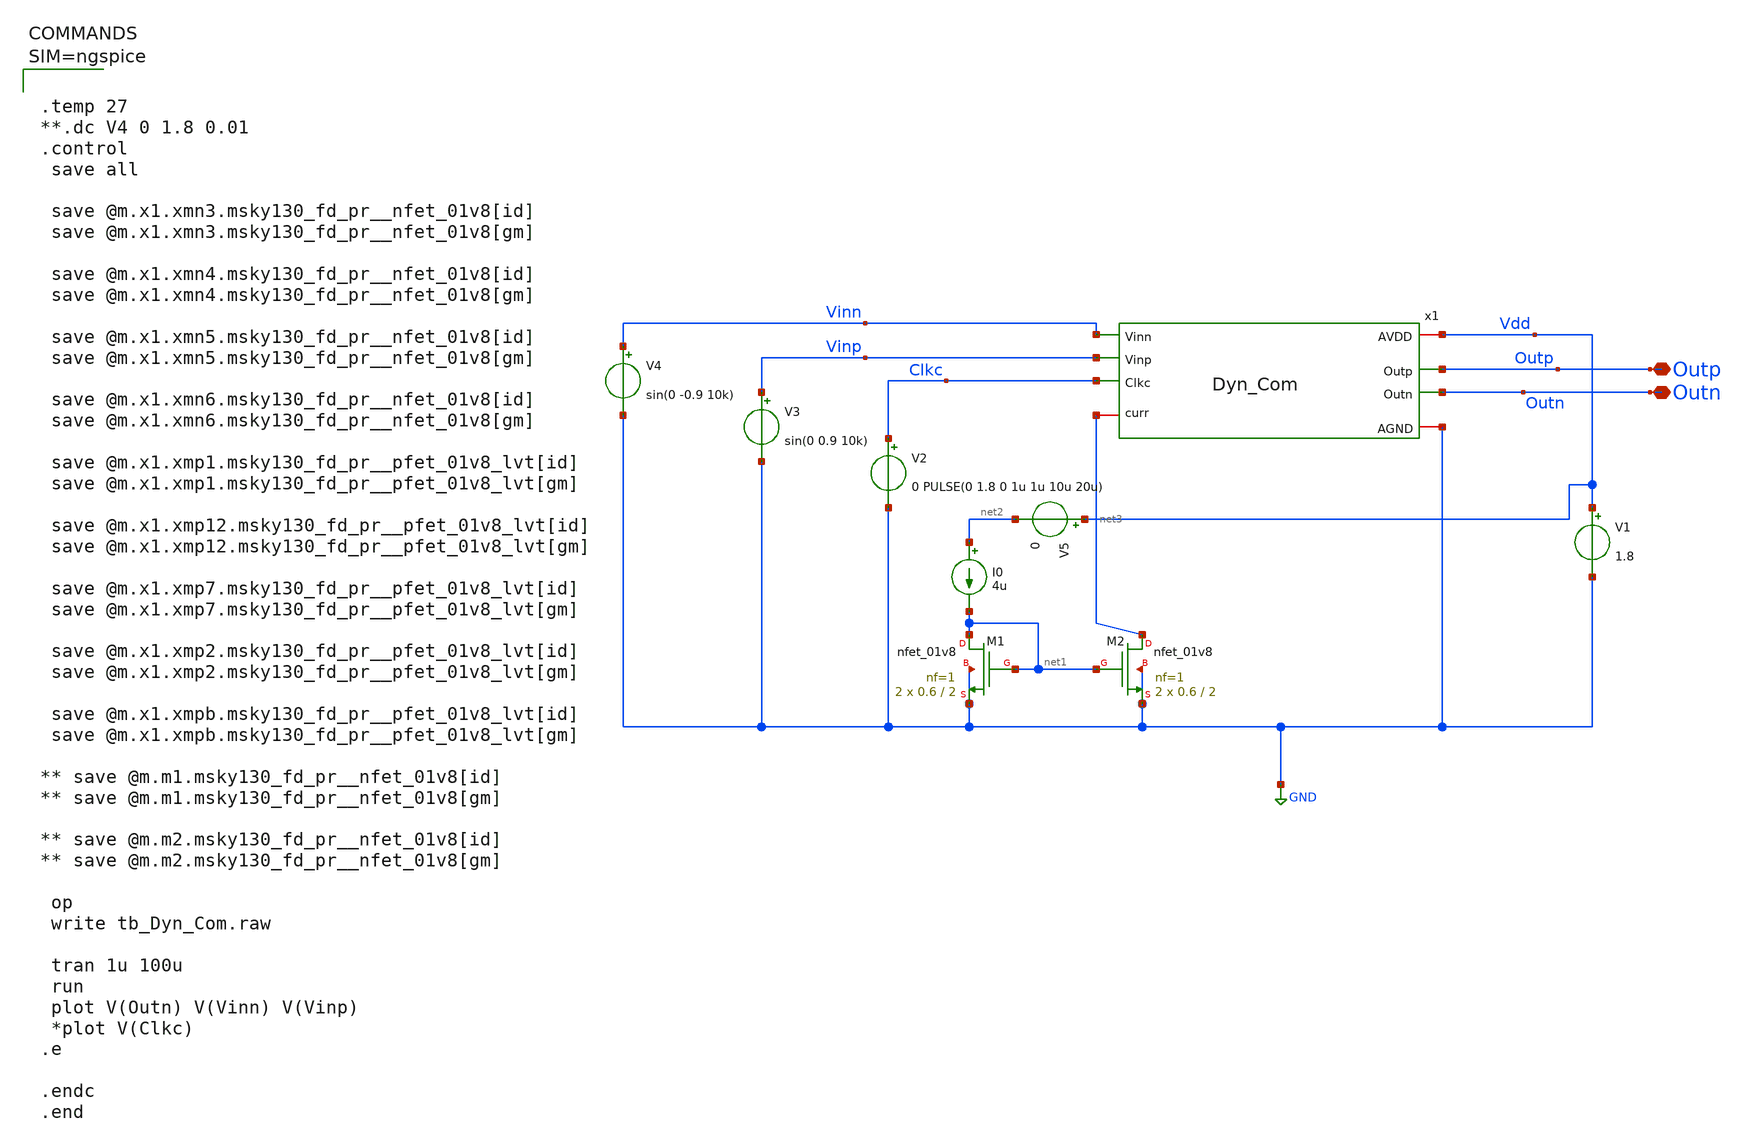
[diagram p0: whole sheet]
** sch_path: sar-adc/updated/tb_Dyn_Com.sch
**.subckt tb_Dyn_Com Outp Outn
*.iopin Outp
*.iopin Outn
x1 Vdd net3 Vinn Vinp Outp Outn Clkc GND Dyn_Com
V4 Vinn GND sin(0 -0.9 10k)
V3 Vinp GND sin(0 0.9 10k)
V2 Clkc GND 0 PULSE(0 1.8 0 1u 1u 10u 20u)
XM2 net3 net1 GND GND sky130_fd_pr__nfet_01v8 L=2 W=0.6 nf=1 ad='int((1 + 1)/2) * 0.6 / 1 * 0.29' as='int((1 + 2)/2) * 0.6 / 1 * 0.29'
+ pd='2*int((1 + 1)/2) * (0.6 / 1 + 0.29)' ps='2*int((1 + 2)/2) * (0.6 / 1 + 0.29)' nrd='0.29 / 0.6 ' nrs='0.29 / 0.6 '
+ sa=0 sb=0 sd=0 mult=2 m=2
XM1 net1 net1 GND GND sky130_fd_pr__nfet_01v8 L=2 W=0.6 nf=1 ad='int((1 + 1)/2) * 0.6 / 1 * 0.29' as='int((1 + 2)/2) * 0.6 / 1 * 0.29'
+ pd='2*int((1 + 1)/2) * (0.6 / 1 + 0.29)' ps='2*int((1 + 2)/2) * (0.6 / 1 + 0.29)' nrd='0.29 / 0.6 ' nrs='0.29 / 0.6 '
+ sa=0 sb=0 sd=0 mult=2 m=2
I0 net2 net1 4u
V5 Vdd net2 0
V1 Vdd GND 1.8
**** begin user architecture code



.temp 27
**.dc V4 0 1.8 0.01
.control
 save all

 save @m.x1.xmn3.msky130_fd_pr__nfet_01v8[id]
 save @m.x1.xmn3.msky130_fd_pr__nfet_01v8[gm]

 save @m.x1.xmn4.msky130_fd_pr__nfet_01v8[id]
 save @m.x1.xmn4.msky130_fd_pr__nfet_01v8[gm]

 save @m.x1.xmn5.msky130_fd_pr__nfet_01v8[id]
 save @m.x1.xmn5.msky130_fd_pr__nfet_01v8[gm]

 save @m.x1.xmn6.msky130_fd_pr__nfet_01v8[id]
 save @m.x1.xmn6.msky130_fd_pr__nfet_01v8[gm]

 save @m.x1.xmp1.msky130_fd_pr__pfet_01v8_lvt[id]
 save @m.x1.xmp1.msky130_fd_pr__pfet_01v8_lvt[gm]

 save @m.x1.xmp12.msky130_fd_pr__pfet_01v8_lvt[id]
 save @m.x1.xmp12.msky130_fd_pr__pfet_01v8_lvt[gm]

 save @m.x1.xmp7.msky130_fd_pr__pfet_01v8_lvt[id]
 save @m.x1.xmp7.msky130_fd_pr__pfet_01v8_lvt[gm]

 save @m.x1.xmp2.msky130_fd_pr__pfet_01v8_lvt[id]
 save @m.x1.xmp2.msky130_fd_pr__pfet_01v8_lvt[gm]

 save @m.x1.xmpb.msky130_fd_pr__pfet_01v8_lvt[id]
 save @m.x1.xmpb.msky130_fd_pr__pfet_01v8_lvt[gm]

** save @m.m1.msky130_fd_pr__nfet_01v8[id]
** save @m.m1.msky130_fd_pr__nfet_01v8[gm]

** save @m.m2.msky130_fd_pr__nfet_01v8[id]
** save @m.m2.msky130_fd_pr__nfet_01v8[gm]

 op
 write tb_Dyn_Com.raw

 tran 1u 100u
 run
 plot V(Outn) V(Vinn) V(Vinp)
 *plot V(Clkc)
.e

.endc
.end




** opencircuitdesign pdks install
.lib $::SKYWATER_MODELS/sky130.lib.spice tt

**** end user architecture code
**.ends

* expanding   symbol:  Dyn_Com.sym # of pins=8
** sym_path: sar-adc/updated/Dyn_Com.sym
** sch_path: sar-adc/updated/Dyn_Com.sch
.subckt Dyn_Com AVDD curr Vinn Vinp Outp Outn Clkc AGND
*.ipin Vinp
*.ipin Vinn
*.opin Outn
*.opin Outp
*.ipin Clkc
*.iopin AVDD
*.iopin AGND
*.iopin curr
XMPB net1 curr AVDD AVDD sky130_fd_pr__pfet_01v8_lvt L=2 W=1.12 nf=1 ad='int((1 + 1)/2) * 1.12 / 1 * 0.29'
+ as='int((1 + 2)/2) * 1.12 / 1 * 0.29' pd='2*int((1 + 1)/2) * (1.12 / 1 + 0.29)' ps='2*int((1 + 2)/2) * (1.12 / 1 + 0.29)'
+ nrd='0.29 / 1.12 ' nrs='0.29 / 1.12 ' sa=0 sb=0 sd=0 mult=4 m=4
XMP7 net2 Clkc net1 AVDD sky130_fd_pr__pfet_01v8_lvt L=2 W=1.12 nf=1 ad='int((1 + 1)/2) * 1.12 / 1 * 0.29'
+ as='int((1 + 2)/2) * 1.12 / 1 * 0.29' pd='2*int((1 + 1)/2) * (1.12 / 1 + 0.29)' ps='2*int((1 + 2)/2) * (1.12 / 1 + 0.29)'
+ nrd='0.29 / 1.12 ' nrs='0.29 / 1.12 ' sa=0 sb=0 sd=0 mult=4 m=4
XMP12 curr curr AVDD AVDD sky130_fd_pr__pfet_01v8_lvt L=2 W=1.12 nf=1 ad='int((1 + 1)/2) * 1.12 / 1 * 0.29'
+ as='int((1 + 2)/2) * 1.12 / 1 * 0.29' pd='2*int((1 + 1)/2) * (1.12 / 1 + 0.29)' ps='2*int((1 + 2)/2) * (1.12 / 1 + 0.29)'
+ nrd='0.29 / 1.12 ' nrs='0.29 / 1.12 ' sa=0 sb=0 sd=0 mult=4 m=4
XMP1 Outp Vinp net2 AVDD sky130_fd_pr__pfet_01v8_lvt L=2 W=2 nf=1 ad='int((1 + 1)/2) * 2 / 1 * 0.29'
+ as='int((1 + 2)/2) * 2 / 1 * 0.29' pd='2*int((1 + 1)/2) * (2 / 1 + 0.29)' ps='2*int((1 + 2)/2) * (2 / 1 + 0.29)'
+ nrd='0.29 / 2 ' nrs='0.29 / 2 ' sa=0 sb=0 sd=0 mult=9 m=9
XMP2 Outn Vinn net2 AVDD sky130_fd_pr__pfet_01v8_lvt L=2 W=2 nf=1 ad='int((1 + 1)/2) * 2 / 1 * 0.29'
+ as='int((1 + 2)/2) * 2 / 1 * 0.29' pd='2*int((1 + 1)/2) * (2 / 1 + 0.29)' ps='2*int((1 + 2)/2) * (2 / 1 + 0.29)'
+ nrd='0.29 / 2 ' nrs='0.29 / 2 ' sa=0 sb=0 sd=0 mult=9 m=9
XMN5 Outp Clkc AGND AGND sky130_fd_pr__nfet_01v8 L=2 W=0.6 nf=1 ad='int((1 + 1)/2) * 0.6 / 1 * 0.29'
+ as='int((1 + 2)/2) * 0.6 / 1 * 0.29' pd='2*int((1 + 1)/2) * (0.6 / 1 + 0.29)' ps='2*int((1 + 2)/2) * (0.6 / 1 + 0.29)'
+ nrd='0.29 / 0.6 ' nrs='0.29 / 0.6 ' sa=0 sb=0 sd=0 mult=2 m=2
XMN3 Outp Outn AGND AGND sky130_fd_pr__nfet_01v8 L=2 W=0.6 nf=1 ad='int((1 + 1)/2) * 0.6 / 1 * 0.29'
+ as='int((1 + 2)/2) * 0.6 / 1 * 0.29' pd='2*int((1 + 1)/2) * (0.6 / 1 + 0.29)' ps='2*int((1 + 2)/2) * (0.6 / 1 + 0.29)'
+ nrd='0.29 / 0.6 ' nrs='0.29 / 0.6 ' sa=0 sb=0 sd=0 mult=2 m=2
XMN4 Outn Outp AGND AGND sky130_fd_pr__nfet_01v8 L=2 W=0.6 nf=1 ad='int((1 + 1)/2) * 0.6 / 1 * 0.29'
+ as='int((1 + 2)/2) * 0.6 / 1 * 0.29' pd='2*int((1 + 1)/2) * (0.6 / 1 + 0.29)' ps='2*int((1 + 2)/2) * (0.6 / 1 + 0.29)'
+ nrd='0.29 / 0.6 ' nrs='0.29 / 0.6 ' sa=0 sb=0 sd=0 mult=2 m=2
XMN6 Outn Clkc AGND AGND sky130_fd_pr__nfet_01v8 L=2 W=0.6 nf=1 ad='int((1 + 1)/2) * 0.6 / 1 * 0.29'
+ as='int((1 + 2)/2) * 0.6 / 1 * 0.29' pd='2*int((1 + 1)/2) * (0.6 / 1 + 0.29)' ps='2*int((1 + 2)/2) * (0.6 / 1 + 0.29)'
+ nrd='0.29 / 0.6 ' nrs='0.29 / 0.6 ' sa=0 sb=0 sd=0 mult=2 m=2
.ends

.GLOBAL GND
.end
